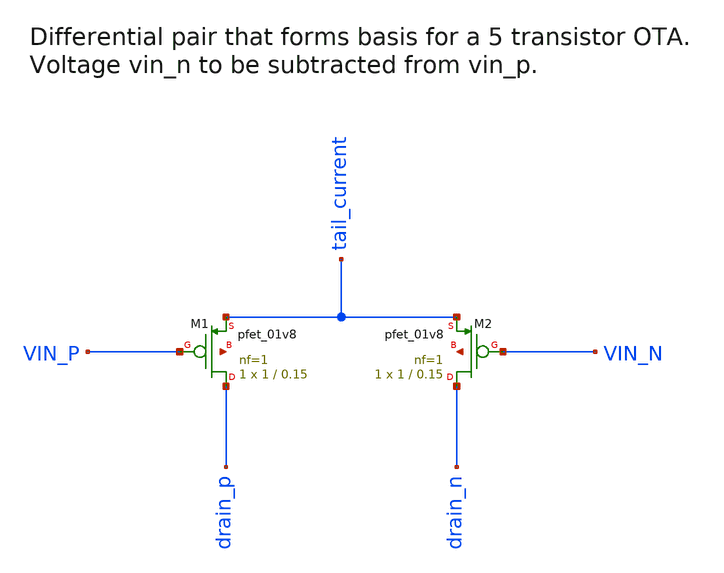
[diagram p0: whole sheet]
** sch_path: xschem/pfet_diff_pair.sch
**.subckt pfet_diff_pair
XM1 drain_p VIN_P tail_current net1 sky130_fd_pr__pfet_01v8 L=0.15 W=1 nf=1 ad='int((1 + 1)/2) * 1 / 1 * 0.29'
+ as='int((1 + 2)/2) * 1 / 1 * 0.29' pd='2*int((1 + 1)/2) * (1 / 1 + 0.29)' ps='2*int((1 + 2)/2) * (1 / 1 + 0.29)'
+ nrd='0.29 / 1 ' nrs='0.29 / 1 ' sa=0 sb=0 sd=0 mult=1 m=1
XM2 drain_n VIN_N tail_current net2 sky130_fd_pr__pfet_01v8 L=0.15 W=1 nf=1 ad='int((1 + 1)/2) * 1 / 1 * 0.29'
+ as='int((1 + 2)/2) * 1 / 1 * 0.29' pd='2*int((1 + 1)/2) * (1 / 1 + 0.29)' ps='2*int((1 + 2)/2) * (1 / 1 + 0.29)'
+ nrd='0.29 / 1 ' nrs='0.29 / 1 ' sa=0 sb=0 sd=0 mult=1 m=1
**.ends
.end
